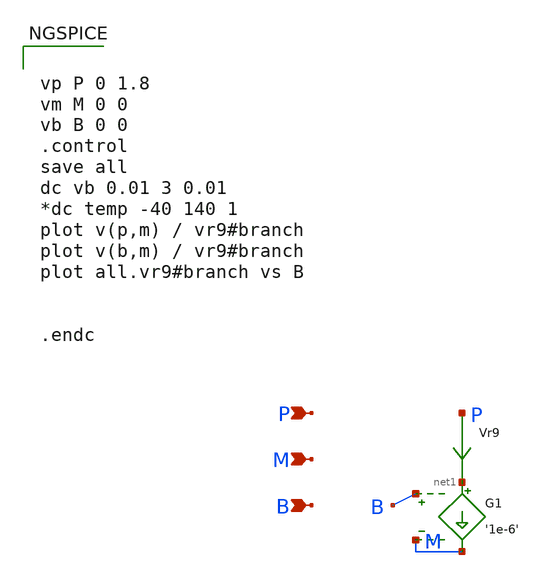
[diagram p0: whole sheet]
** sch_path: test_vccs.sch
* Copyright 2020 Stefan Frederik Schippers
* Licensed under the Apache License, Version 2.0 (the "License");
* you may not use this file except in compliance with the License.
* You may obtain a copy of the License at
* https://www.apache.org/licenses/LICENSE-2.0
* Unless required by applicable law or agreed to in writing, software
* distributed under the License is distributed on an "AS IS" BASIS,
* WITHOUT WARRANTIES OR CONDITIONS OF ANY KIND, either express or implied.
* See the License for the specific language governing permissions and
* limitations under the License.
**.subckt test_vccs P M B
*.ipin P
*.ipin M
*.ipin B
Vr9 P net1 0
.save i(vr9)
G1 net1 M B M '1e-6'
**** begin user architecture code


vp P 0 1.8
vm M 0 0
vb B 0 0
.control
save all
dc vb 0.01 3 0.01
*dc temp -40 140 1
plot v(p,m) / vr9#branch
plot v(b,m) / vr9#branch
plot all.vr9#branch vs B


.endc


 .lib $::SKYWATER_MODELS/models/sky130.lib.spice tt

.param mc_mm_switch=0
.param mc_pr_switch=1


**** end user architecture code
**.ends
.end
